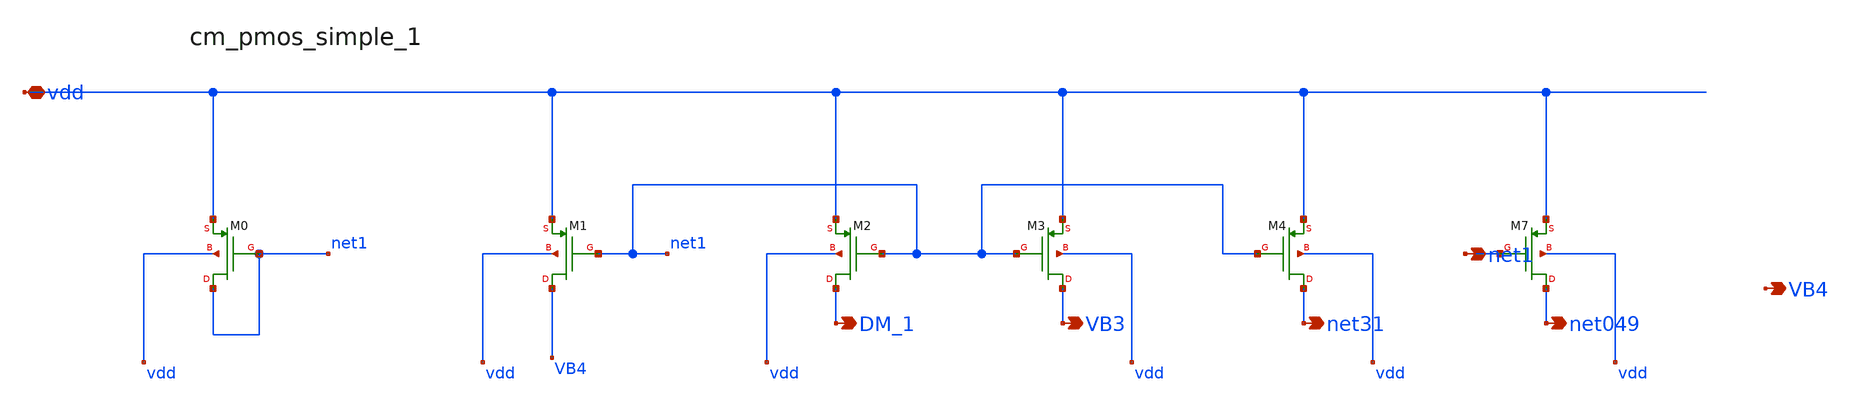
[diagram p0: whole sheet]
** sch_path: analog-db/raw/amp_007_leung_dfcfc2/hier/blocks/cm_pmos_simple_1.sch
**.subckt cm_pmos_simple_1 vdd net1 DM_1 VB3 net31 net049 VB4
*.iopin vdd
*.opin net1
*.opin DM_1
*.opin VB3
*.opin net31
*.opin net049
*.opin VB4
XM0 net1 net1 vdd vdd sg13_lv_pmos w=x_dut_xm0_w l=x_dut_xm0_l ng=1 m=x_dut_xm0_m
XM1 VB4 net1 vdd vdd sg13_lv_pmos w=x_dut_xm1_w l=x_dut_xm1_l ng=1 m=x_dut_xm1_m
XM2 DM_1 net1 vdd vdd sg13_lv_pmos w=x_dut_xm2_w l=x_dut_xm2_l ng=1 m=x_dut_xm2_m
XM3 VB3 net1 vdd vdd sg13_lv_pmos w=x_dut_xm3_w l=x_dut_xm3_l ng=1 m=x_dut_xm3_m
XM4 net31 net1 vdd vdd sg13_lv_pmos w=x_dut_xm4_w l=x_dut_xm4_l ng=1 m=x_dut_xm4_m
XM7 net049 net1 vdd vdd sg13_lv_pmos w=x_dut_xm7_w l=x_dut_xm7_l ng=1 m=x_dut_xm7_m
**.ends
.end
